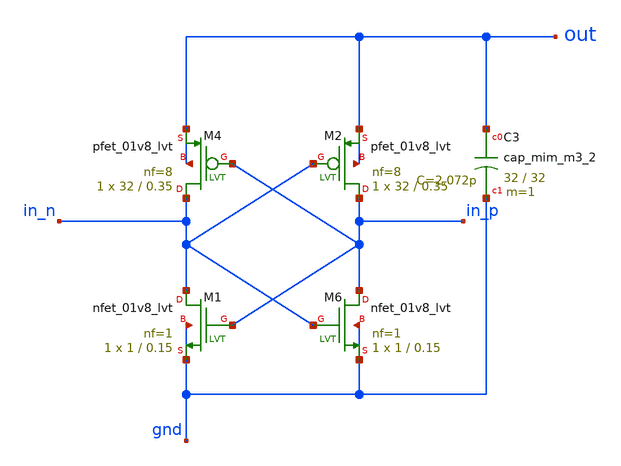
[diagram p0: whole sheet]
** sch_path: src/rectifier_schematic.sch
**.subckt rectifier_schematic
XM4 in_n in_p out out sky130_fd_pr__pfet_01v8_lvt L=0.35 W=32 nf=8 ad='int((8 + 1)/2) * 32 / 8 * 0.29'
+ as='int((8 + 2)/2) * 32 / 8 * 0.29' pd='2*int((8 + 1)/2) * (32 / 8 + 0.29)' ps='2*int((8 + 2)/2) * (32 / 8 + 0.29)'
+ nrd='0.29 / 32 ' nrs='0.29 / 32 ' sa=0 sb=0 sd=0 mult=1 m=1
XM2 in_p in_n out out sky130_fd_pr__pfet_01v8_lvt L=0.35 W=32 nf=8 ad='int((8 + 1)/2) * 32 / 8 * 0.29'
+ as='int((8 + 2)/2) * 32 / 8 * 0.29' pd='2*int((8 + 1)/2) * (32 / 8 + 0.29)' ps='2*int((8 + 2)/2) * (32 / 8 + 0.29)'
+ nrd='0.29 / 32 ' nrs='0.29 / 32 ' sa=0 sb=0 sd=0 mult=1 m=1
XM6 in_p in_n gnd gnd sky130_fd_pr__nfet_01v8_lvt L=0.15 W=1 nf=1 ad='int((1 + 1)/2) * 1 / 1 * 0.29'
+ as='int((1 + 2)/2) * 1 / 1 * 0.29' pd='2*int((1 + 1)/2) * (1 / 1 + 0.29)' ps='2*int((1 + 2)/2) * (1 / 1 + 0.29)'
+ nrd='0.29 / 1 ' nrs='0.29 / 1 ' sa=0 sb=0 sd=0 mult=1 m=1
XM1 in_n in_p gnd gnd sky130_fd_pr__nfet_01v8_lvt L=0.15 W=1 nf=1 ad='int((1 + 1)/2) * 1 / 1 * 0.29'
+ as='int((1 + 2)/2) * 1 / 1 * 0.29' pd='2*int((1 + 1)/2) * (1 / 1 + 0.29)' ps='2*int((1 + 2)/2) * (1 / 1 + 0.29)'
+ nrd='0.29 / 1 ' nrs='0.29 / 1 ' sa=0 sb=0 sd=0 mult=1 m=1
XC3 out gnd sky130_fd_pr__cap_mim_m3_2 W=32 L=32 MF=1 m=1
**.ends
.end
